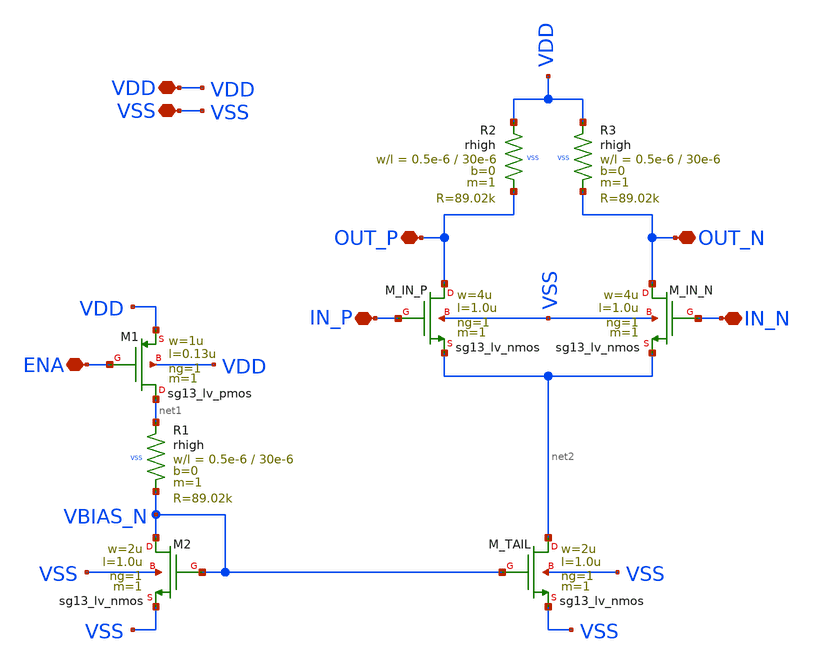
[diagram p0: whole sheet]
** sch_path: xschem/Small_Differential_Amplifier.sch
**.subckt Small_Differential_Amplifier VDD IN_N IN_P OUT_N VSS OUT_P ENA
*.iopin VDD
*.iopin IN_N
*.iopin IN_P
*.iopin OUT_N
*.iopin VSS
*.iopin OUT_P
*.iopin ENA
XM2 VBIAS_N VBIAS_N VSS VSS sg13_lv_nmos w=2u l=1.0u ng=1 m=1 mm_ok=1
XR1 net1 VBIAS_N VSS rhigh w=0.5e-6 l=30e-6 m=1 b=0 mm_ok=1
XM_TAIL net2 VBIAS_N VSS VSS sg13_lv_nmos w=2u l=1.0u ng=1 m=1 mm_ok=1
XM_IN_P OUT_P IN_P net2 VSS sg13_lv_nmos w=4u l=1.0u ng=1 m=1 mm_ok=1
XM_IN_N OUT_N IN_N net2 VSS sg13_lv_nmos w=4u l=1.0u ng=1 m=1 mm_ok=1
XR2 VDD OUT_P VSS rhigh w=0.5e-6 l=30e-6 m=1 b=0 mm_ok=1
XR3 VDD OUT_N VSS rhigh w=0.5e-6 l=30e-6 m=1 b=0 mm_ok=1
XM1 net1 ENA VDD VDD sg13_lv_pmos w=1u l=0.13u ng=1 m=1 mm_ok=1
**.ends
.end
